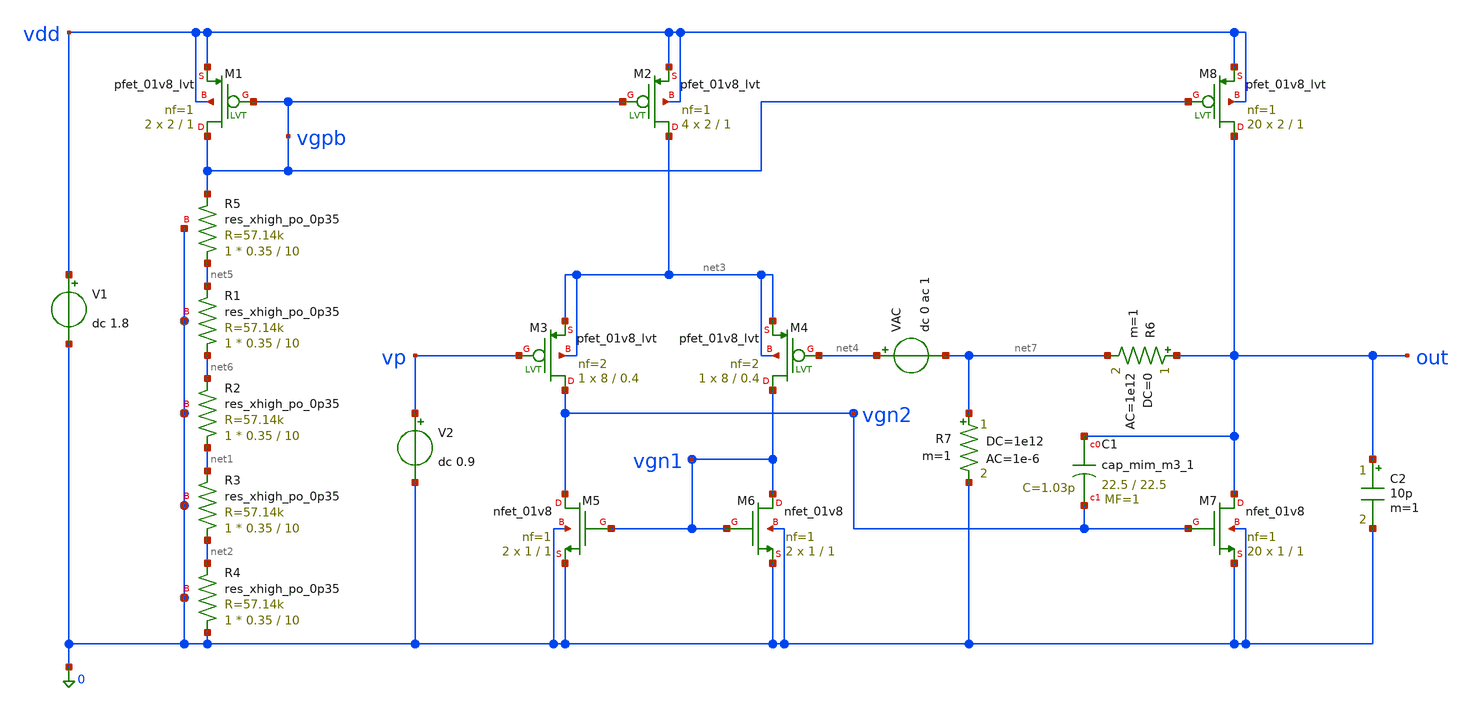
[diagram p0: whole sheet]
** sch_path: example_sch/opamp_ac.sch
**.subckt opamp_ac
XR2 net1 net6 0 sky130_fd_pr__res_xhigh_po_0p35 L=10 mult=1 m=1
XR3 net2 net1 0 sky130_fd_pr__res_xhigh_po_0p35 L=10 mult=1 m=1
XR4 0 net2 0 sky130_fd_pr__res_xhigh_po_0p35 L=10 mult=1 m=1
V1 vdd 0 dc 1.8
V2 vp 0 dc 0.9
XM5 vgn2 vgn1 0 0 sky130_fd_pr__nfet_01v8 L=1 W=1 nf=1 ad='int((nf+1)/2) * W/nf * 0.29' as='int((nf+2)/2) * W/nf * 0.29'
+ pd='2*int((nf+1)/2) * (W/nf + 0.29)' ps='2*int((nf+2)/2) * (W/nf + 0.29)' nrd='0.29 / W' nrs='0.29 / W'
+ sa=0 sb=0 sd=0 mult=2 m=2
XM6 vgn1 vgn1 0 0 sky130_fd_pr__nfet_01v8 L=1 W=1 nf=1 ad='int((nf+1)/2) * W/nf * 0.29' as='int((nf+2)/2) * W/nf * 0.29'
+ pd='2*int((nf+1)/2) * (W/nf + 0.29)' ps='2*int((nf+2)/2) * (W/nf + 0.29)' nrd='0.29 / W' nrs='0.29 / W'
+ sa=0 sb=0 sd=0 mult=2 m=2
XM7 out vgn2 0 0 sky130_fd_pr__nfet_01v8 L=1 W=1 nf=1 ad='int((nf+1)/2) * W/nf * 0.29' as='int((nf+2)/2) * W/nf * 0.29'
+ pd='2*int((nf+1)/2) * (W/nf + 0.29)' ps='2*int((nf+2)/2) * (W/nf + 0.29)' nrd='0.29 / W' nrs='0.29 / W'
+ sa=0 sb=0 sd=0 mult=20 m=20
XR1 net6 net5 0 sky130_fd_pr__res_xhigh_po_0p35 L=10 mult=1 m=1
XR5 net5 vgpb 0 sky130_fd_pr__res_xhigh_po_0p35 L=10 mult=1 m=1
XM1 vgpb vgpb vdd vdd sky130_fd_pr__pfet_01v8_lvt L=1 W=2 nf=1 ad='int((nf+1)/2) * W/nf * 0.29' as='int((nf+2)/2) * W/nf * 0.29'
+ pd='2*int((nf+1)/2) * (W/nf + 0.29)' ps='2*int((nf+2)/2) * (W/nf + 0.29)' nrd='0.29 / W' nrs='0.29 / W'
+ sa=0 sb=0 sd=0 mult=2 m=2
XM2 net3 vgpb vdd vdd sky130_fd_pr__pfet_01v8_lvt L=1 W=2 nf=1 ad='int((nf+1)/2) * W/nf * 0.29' as='int((nf+2)/2) * W/nf * 0.29'
+ pd='2*int((nf+1)/2) * (W/nf + 0.29)' ps='2*int((nf+2)/2) * (W/nf + 0.29)' nrd='0.29 / W' nrs='0.29 / W'
+ sa=0 sb=0 sd=0 mult=4 m=4
XM8 out vgpb vdd vdd sky130_fd_pr__pfet_01v8_lvt L=1 W=2 nf=1 ad='int((nf+1)/2) * W/nf * 0.29' as='int((nf+2)/2) * W/nf * 0.29'
+ pd='2*int((nf+1)/2) * (W/nf + 0.29)' ps='2*int((nf+2)/2) * (W/nf + 0.29)' nrd='0.29 / W' nrs='0.29 / W'
+ sa=0 sb=0 sd=0 mult=20 m=20
XM3 vgn2 vp net3 net3 sky130_fd_pr__pfet_01v8_lvt L=0.4 W=8 nf=2 ad='int((nf+1)/2) * W/nf * 0.29' as='int((nf+2)/2) * W/nf * 0.29'
+ pd='2*int((nf+1)/2) * (W/nf + 0.29)' ps='2*int((nf+2)/2) * (W/nf + 0.29)' nrd='0.29 / W' nrs='0.29 / W'
+ sa=0 sb=0 sd=0 mult=1 m=1
XM4 vgn1 net4 net3 net3 sky130_fd_pr__pfet_01v8_lvt L=0.4 W=8 nf=2 ad='int((nf+1)/2) * W/nf * 0.29' as='int((nf+2)/2) * W/nf * 0.29'
+ pd='2*int((nf+1)/2) * (W/nf + 0.29)' ps='2*int((nf+2)/2) * (W/nf + 0.29)' nrd='0.29 / W' nrs='0.29 / W'
+ sa=0 sb=0 sd=0 mult=1 m=1
R6 out net7 0 ac=1e12 m=1
R7 net7 0 1e12 ac=1e-6 m=1
VAC net4 net7 dc 0 ac 1
XC1 out vgn2 sky130_fd_pr__cap_mim_m3_1 W=22.5 L=22.5 MF=1 m=1
C2 out 0 10p m=1
**** begin user architecture code

** opencircuitdesign pdks install
.lib $::SKYWATER_MODELS/sky130.lib.spice tt


**** end user architecture code
**.ends
**** begin user architecture code


*** Save all devices' currents ***
*.options savecurrents

*** Save all voltages	and others ***
*.save all
*.save @m.xm3.msky130_fd_pr__pfet_01v8_lvt[gm]
*.save @m.xm4.msky130_fd_pr__pfet_01v8_lvt[gm]
*.save @m.xm7.msky130_fd_pr__nfet_01v8[gm]

**** Control statements for simulation ****
*   .control <-- start of control statement
*   ac dec 10 1 100k <-- calcuate ac response
*   let xx=yy        <-- assign xx to represent the yy
*   write    <-- write results into a RAW file
*   meas ... <-- measure the ac result to find the gain margin and phase margin
*   quit     <-- leave simulation
*   .endc    <-- end of control statement
********************************************
.control
ac dec 20 10 100e6
let db_out=vdb(out)
let p_out=cph(out)*180/pi
write
meas ac phase_margin(deg) find p_out when db_out=0
meas ac gain_margin(db) find db_out when p_out=0
quit
.endc


**** end user architecture code
.end
